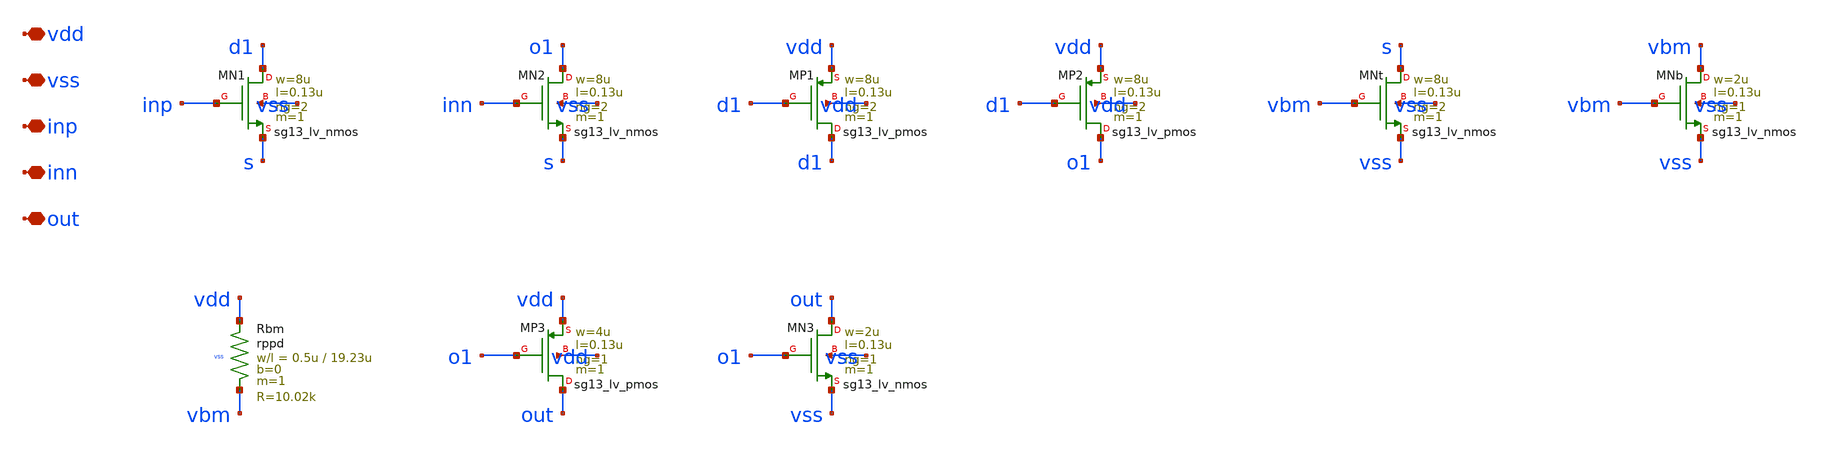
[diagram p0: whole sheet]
** sch_path: design/tx/tx_lvl_cml2cmos.sch
**.subckt tx_lvl_cml2cmos vdd vss inp inn out
*.iopin vdd
*.iopin vss
*.iopin inp
*.iopin inn
*.iopin out
XMN1 d1 inp s vss sg13_lv_nmos w=8u l=0.13u ng=2 m=1 mm_ok=1
XMN2 o1 inn s vss sg13_lv_nmos w=8u l=0.13u ng=2 m=1 mm_ok=1
XMP1 d1 d1 vdd vdd sg13_lv_pmos w=8u l=0.13u ng=2 m=1 mm_ok=1
XMP2 o1 d1 vdd vdd sg13_lv_pmos w=8u l=0.13u ng=2 m=1 mm_ok=1
XMNt s vbm vss vss sg13_lv_nmos w=8u l=0.13u ng=2 m=1 mm_ok=1
XMNb vbm vbm vss vss sg13_lv_nmos w=2u l=0.13u ng=1 m=1 mm_ok=1
XRbm vdd vbm vss rppd w=0.5u l=19.23u m=1 b=0 mm_ok=1
XMP3 out o1 vdd vdd sg13_lv_pmos w=4u l=0.13u ng=1 m=1 mm_ok=1
XMN3 out o1 vss vss sg13_lv_nmos w=2u l=0.13u ng=1 m=1 mm_ok=1
**.ends
.end
